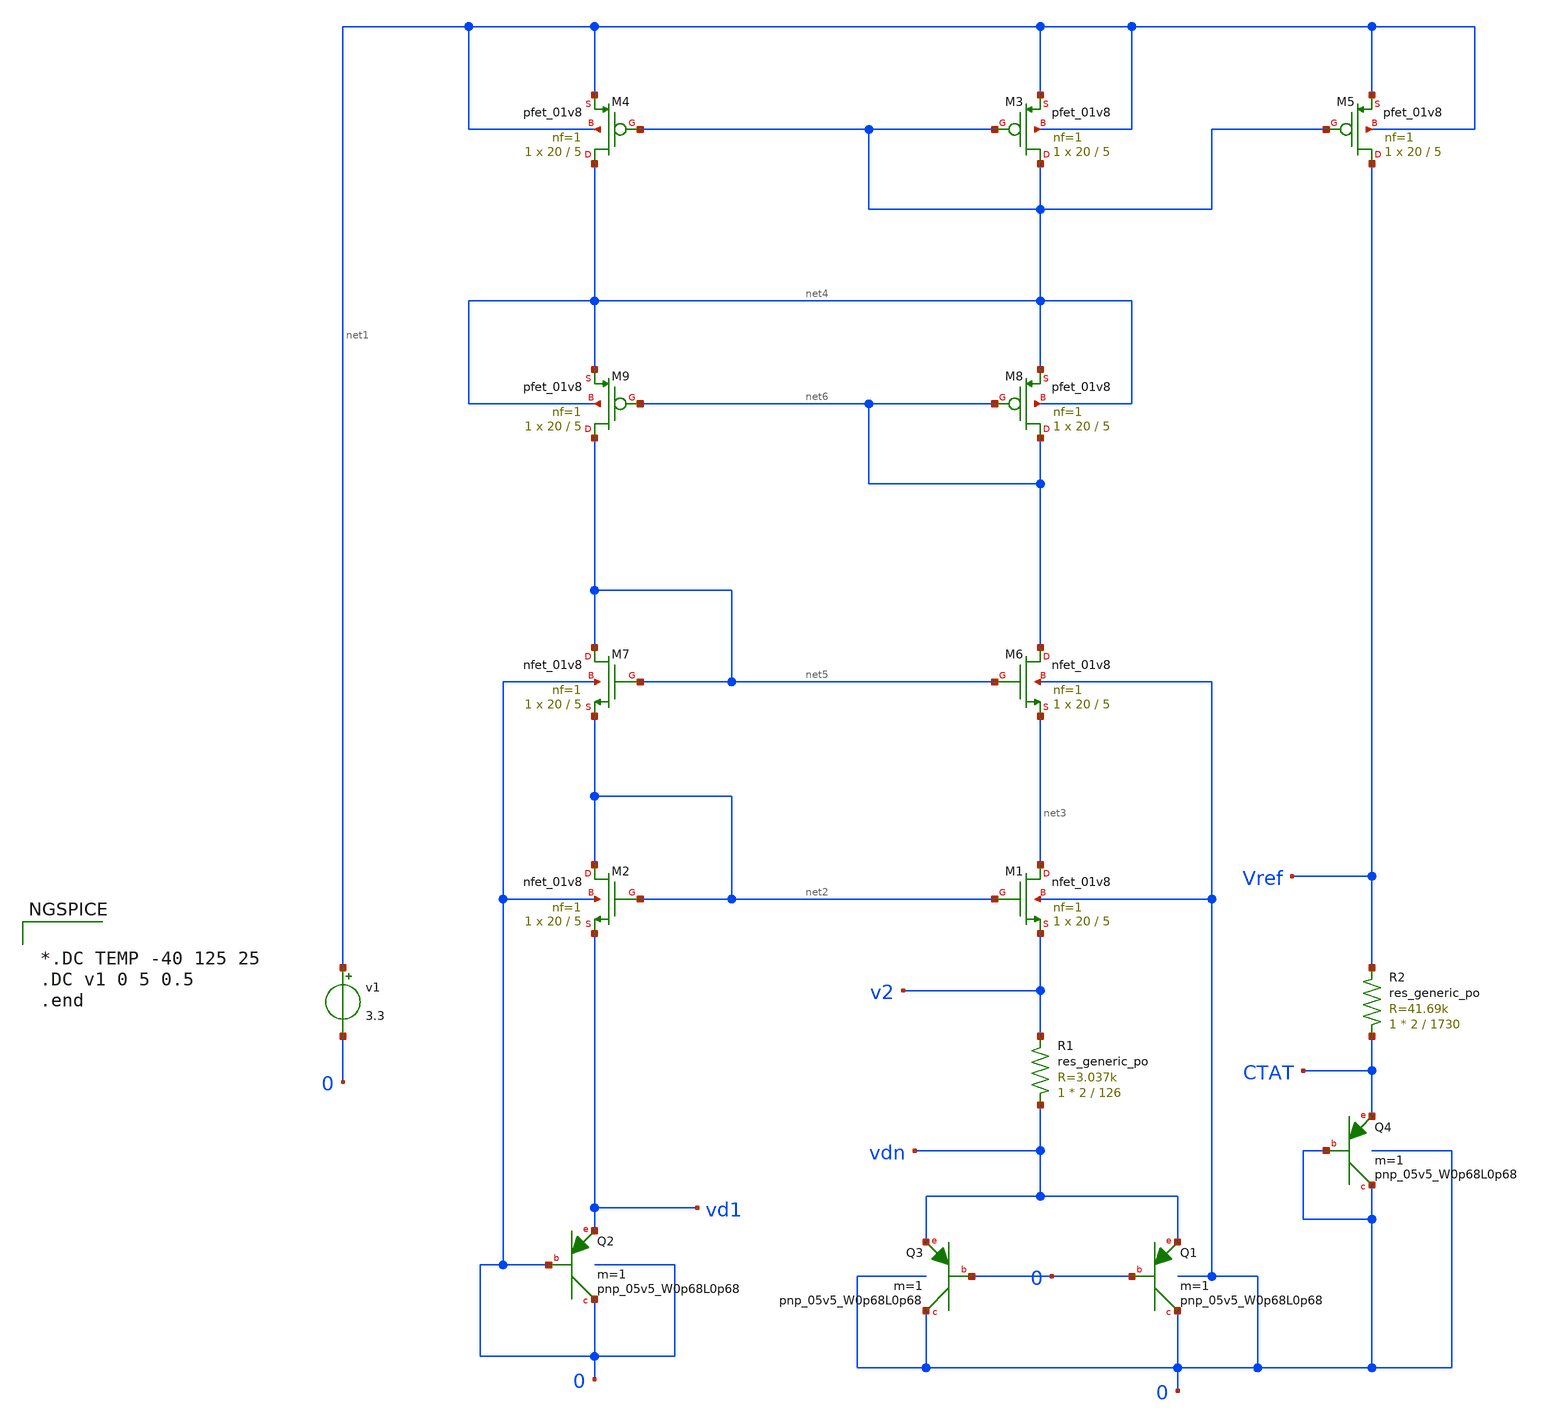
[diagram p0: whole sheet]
** sch_path: Bandgap/PTAT_CTAT_Cascode_CM.sch
**.subckt PTAT_CTAT_Cascode_CM
v1 net1 0 3.3
XQ2 0 0 vd1 sky130_fd_pr__pnp_05v5_W0p68L0p68 m=1
XQ1 0 0 vdn sky130_fd_pr__pnp_05v5_W0p68L0p68 m=1
XQ3 0 0 vdn sky130_fd_pr__pnp_05v5_W0p68L0p68 m=1
XM1 net3 net2 v2 0 sky130_fd_pr__nfet_01v8 L=5 W=20 nf=1 ad='int((nf+1)/2) * W/nf * 0.29' as='int((nf+2)/2) * W/nf * 0.29'
+ pd='2*int((nf+1)/2) * (W/nf + 0.29)' ps='2*int((nf+2)/2) * (W/nf + 0.29)' nrd='0.29 / W' nrs='0.29 / W'
+ sa=0 sb=0 sd=0 mult=1 m=1
XM2 net2 net2 vd1 0 sky130_fd_pr__nfet_01v8 L=5 W=20 nf=1 ad='int((nf+1)/2) * W/nf * 0.29' as='int((nf+2)/2) * W/nf * 0.29'
+ pd='2*int((nf+1)/2) * (W/nf + 0.29)' ps='2*int((nf+2)/2) * (W/nf + 0.29)' nrd='0.29 / W' nrs='0.29 / W'
+ sa=0 sb=0 sd=0 mult=1 m=1
XM3 net4 net4 net1 net1 sky130_fd_pr__pfet_01v8 L=5 W=20 nf=1 ad='int((nf+1)/2) * W/nf * 0.29' as='int((nf+2)/2) * W/nf * 0.29'
+ pd='2*int((nf+1)/2) * (W/nf + 0.29)' ps='2*int((nf+2)/2) * (W/nf + 0.29)' nrd='0.29 / W' nrs='0.29 / W'
+ sa=0 sb=0 sd=0 mult=1 m=1
XM4 net4 net4 net1 net1 sky130_fd_pr__pfet_01v8 L=5 W=20 nf=1 ad='int((nf+1)/2) * W/nf * 0.29' as='int((nf+2)/2) * W/nf * 0.29'
+ pd='2*int((nf+1)/2) * (W/nf + 0.29)' ps='2*int((nf+2)/2) * (W/nf + 0.29)' nrd='0.29 / W' nrs='0.29 / W'
+ sa=0 sb=0 sd=0 mult=1 m=1
XM5 Vref net4 net1 net1 sky130_fd_pr__pfet_01v8 L=5 W=20 nf=1 ad='int((nf+1)/2) * W/nf * 0.29' as='int((nf+2)/2) * W/nf * 0.29'
+ pd='2*int((nf+1)/2) * (W/nf + 0.29)' ps='2*int((nf+2)/2) * (W/nf + 0.29)' nrd='0.29 / W' nrs='0.29 / W'
+ sa=0 sb=0 sd=0 mult=1 m=1
XQ4 0 0 CTAT sky130_fd_pr__pnp_05v5_W0p68L0p68 m=1
XR1 vdn v2 sky130_fd_pr__res_generic_po W=2 L=126 m=1
XR2 CTAT Vref sky130_fd_pr__res_generic_po W=2 L=1730 m=1
XM6 net6 net5 net3 0 sky130_fd_pr__nfet_01v8 L=5 W=20 nf=1 ad='int((nf+1)/2) * W/nf * 0.29' as='int((nf+2)/2) * W/nf * 0.29'
+ pd='2*int((nf+1)/2) * (W/nf + 0.29)' ps='2*int((nf+2)/2) * (W/nf + 0.29)' nrd='0.29 / W' nrs='0.29 / W'
+ sa=0 sb=0 sd=0 mult=1 m=1
XM7 net5 net5 net2 0 sky130_fd_pr__nfet_01v8 L=5 W=20 nf=1 ad='int((nf+1)/2) * W/nf * 0.29' as='int((nf+2)/2) * W/nf * 0.29'
+ pd='2*int((nf+1)/2) * (W/nf + 0.29)' ps='2*int((nf+2)/2) * (W/nf + 0.29)' nrd='0.29 / W' nrs='0.29 / W'
+ sa=0 sb=0 sd=0 mult=1 m=1
XM8 net6 net6 net4 net4 sky130_fd_pr__pfet_01v8 L=5 W=20 nf=1 ad='int((nf+1)/2) * W/nf * 0.29' as='int((nf+2)/2) * W/nf * 0.29'
+ pd='2*int((nf+1)/2) * (W/nf + 0.29)' ps='2*int((nf+2)/2) * (W/nf + 0.29)' nrd='0.29 / W' nrs='0.29 / W'
+ sa=0 sb=0 sd=0 mult=1 m=1
XM9 net5 net6 net4 net4 sky130_fd_pr__pfet_01v8 L=5 W=20 nf=1 ad='int((nf+1)/2) * W/nf * 0.29' as='int((nf+2)/2) * W/nf * 0.29'
+ pd='2*int((nf+1)/2) * (W/nf + 0.29)' ps='2*int((nf+2)/2) * (W/nf + 0.29)' nrd='0.29 / W' nrs='0.29 / W'
+ sa=0 sb=0 sd=0 mult=1 m=1
**** begin user architecture code

.include $::SKYWATER_MODELS/cells/nfet_01v8/sky130_fd_pr__nfet_01v8__tt.corner.spice
.include $::SKYWATER_MODELS/cells/nfet_01v8_lvt/sky130_fd_pr__nfet_01v8_lvt__tt.corner.spice
.include $::SKYWATER_MODELS/cells/pfet_01v8/sky130_fd_pr__pfet_01v8__tt.corner.spice
.include $::SKYWATER_MODELS/cells/nfet_03v3_nvt/sky130_fd_pr__nfet_03v3_nvt__tt.corner.spice
.include $::SKYWATER_MODELS/cells/nfet_05v0_nvt/sky130_fd_pr__nfet_05v0_nvt__tt.corner.spice
.include $::SKYWATER_MODELS/cells/esd_nfet_01v8/sky130_fd_pr__esd_nfet_01v8__tt.corner.spice
.include $::SKYWATER_MODELS/cells/pfet_01v8_lvt/sky130_fd_pr__pfet_01v8_lvt__tt.corner.spice
.include $::SKYWATER_MODELS/cells/pfet_01v8_hvt/sky130_fd_pr__pfet_01v8_hvt__tt.corner.spice
.include $::SKYWATER_MODELS/cells/esd_pfet_g5v0d10v5/sky130_fd_pr__esd_pfet_g5v0d10v5__tt.corner.spice
.include $::SKYWATER_MODELS/cells/pfet_g5v0d10v5/sky130_fd_pr__pfet_g5v0d10v5__tt.corner.spice
.include $::SKYWATER_MODELS/cells/pfet_g5v0d16v0/sky130_fd_pr__pfet_g5v0d16v0__tt.corner.spice
.include $::SKYWATER_MODELS/cells/nfet_g5v0d10v5/sky130_fd_pr__nfet_g5v0d10v5__tt.corner.spice
.include $::SKYWATER_MODELS/cells/nfet_g5v0d16v0/sky130_fd_pr__nfet_g5v0d16v0__tt_discrete.corner.spice
.include $::SKYWATER_MODELS/cells/esd_nfet_g5v0d10v5/sky130_fd_pr__esd_nfet_g5v0d10v5__tt.corner.spice
.include $::SKYWATER_MODELS/models/corners/tt/nonfet.spice
* Mismatch parameters
.include $::SKYWATER_MODELS/cells/nfet_01v8/sky130_fd_pr__nfet_01v8__mismatch.corner.spice
.include $::SKYWATER_MODELS/cells/pfet_01v8/sky130_fd_pr__pfet_01v8__mismatch.corner.spice
.include $::SKYWATER_MODELS/cells/nfet_01v8_lvt/sky130_fd_pr__nfet_01v8_lvt__mismatch.corner.spice
.include $::SKYWATER_MODELS/cells/pfet_01v8_lvt/sky130_fd_pr__pfet_01v8_lvt__mismatch.corner.spice
.include $::SKYWATER_MODELS/cells/pfet_01v8_hvt/sky130_fd_pr__pfet_01v8_hvt__mismatch.corner.spice
.include $::SKYWATER_MODELS/cells/nfet_g5v0d10v5/sky130_fd_pr__nfet_g5v0d10v5__mismatch.corner.spice
.include $::SKYWATER_MODELS/cells/pfet_g5v0d10v5/sky130_fd_pr__pfet_g5v0d10v5__mismatch.corner.spice
.include $::SKYWATER_MODELS/cells/nfet_05v0_nvt/sky130_fd_pr__nfet_05v0_nvt__mismatch.corner.spice
.include $::SKYWATER_MODELS/cells/nfet_03v3_nvt/sky130_fd_pr__nfet_03v3_nvt__mismatch.corner.spice
* Resistor$::SKYWATER_MODELS/Capacitor
.include $::SKYWATER_MODELS/models/r+c/res_typical__cap_typical.spice
.include $::SKYWATER_MODELS/models/r+c/res_typical__cap_typical__lin.spice
* Special cells
.include $::SKYWATER_MODELS/models/corners/tt/specialized_cells.spice
* All models
.include $::SKYWATER_MODELS/models/all.spice
* Corner
.include $::SKYWATER_MODELS/models/corners/tt/rf.spice



*.DC TEMP -40 125 25
.DC v1 0 5 0.5
.end


**** end user architecture code
**.ends
.end
